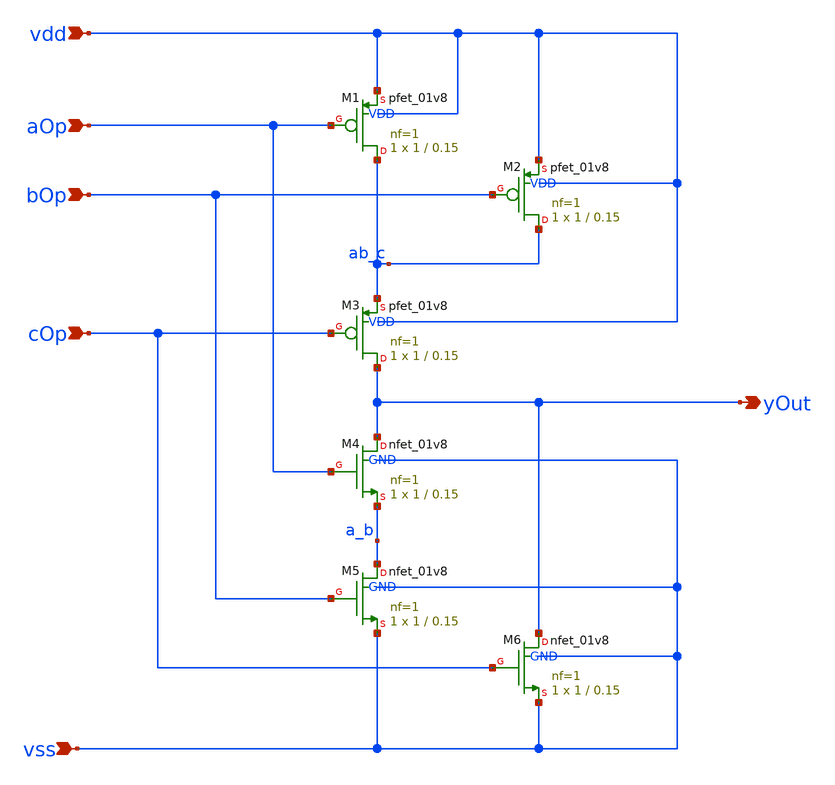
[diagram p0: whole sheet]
** sch_path: xschem/nAbPlC.sch
**.subckt nAbPlC aOp bOp cOp vdd vss yOut
*.ipin aOp
*.ipin bOp
*.ipin cOp
*.ipin vdd
*.ipin vss
*.opin yOut
XM1 ab_c aOp vdd VDD sky130_fd_pr__pfet_01v8 L=0.15 W=1 nf=1 ad='int((nf+1)/2) * W/nf * 0.29' as='int((nf+2)/2) * W/nf * 0.29'
+ pd='2*int((nf+1)/2) * (W/nf + 0.29)' ps='2*int((nf+2)/2) * (W/nf + 0.29)' nrd='0.29 / W' nrs='0.29 / W'
+ sa=0 sb=0 sd=0 mult=1 m=1
XM2 ab_c bOp vdd VDD sky130_fd_pr__pfet_01v8 L=0.15 W=1 nf=1 ad='int((nf+1)/2) * W/nf * 0.29' as='int((nf+2)/2) * W/nf * 0.29'
+ pd='2*int((nf+1)/2) * (W/nf + 0.29)' ps='2*int((nf+2)/2) * (W/nf + 0.29)' nrd='0.29 / W' nrs='0.29 / W'
+ sa=0 sb=0 sd=0 mult=1 m=1
XM3 yOut cOp ab_c VDD sky130_fd_pr__pfet_01v8 L=0.15 W=1 nf=1 ad='int((nf+1)/2) * W/nf * 0.29' as='int((nf+2)/2) * W/nf * 0.29'
+ pd='2*int((nf+1)/2) * (W/nf + 0.29)' ps='2*int((nf+2)/2) * (W/nf + 0.29)' nrd='0.29 / W' nrs='0.29 / W'
+ sa=0 sb=0 sd=0 mult=1 m=1
XM4 yOut aOp a_b GND sky130_fd_pr__nfet_01v8 L=0.15 W=1 nf=1 ad='int((nf+1)/2) * W/nf * 0.29' as='int((nf+2)/2) * W/nf * 0.29'
+ pd='2*int((nf+1)/2) * (W/nf + 0.29)' ps='2*int((nf+2)/2) * (W/nf + 0.29)' nrd='0.29 / W' nrs='0.29 / W'
+ sa=0 sb=0 sd=0 mult=1 m=1
XM5 a_b bOp vss GND sky130_fd_pr__nfet_01v8 L=0.15 W=1 nf=1 ad='int((nf+1)/2) * W/nf * 0.29' as='int((nf+2)/2) * W/nf * 0.29'
+ pd='2*int((nf+1)/2) * (W/nf + 0.29)' ps='2*int((nf+2)/2) * (W/nf + 0.29)' nrd='0.29 / W' nrs='0.29 / W'
+ sa=0 sb=0 sd=0 mult=1 m=1
XM6 yOut cOp vss GND sky130_fd_pr__nfet_01v8 L=0.15 W=1 nf=1 ad='int((nf+1)/2) * W/nf * 0.29' as='int((nf+2)/2) * W/nf * 0.29'
+ pd='2*int((nf+1)/2) * (W/nf + 0.29)' ps='2*int((nf+2)/2) * (W/nf + 0.29)' nrd='0.29 / W' nrs='0.29 / W'
+ sa=0 sb=0 sd=0 mult=1 m=1
**.ends
.end
